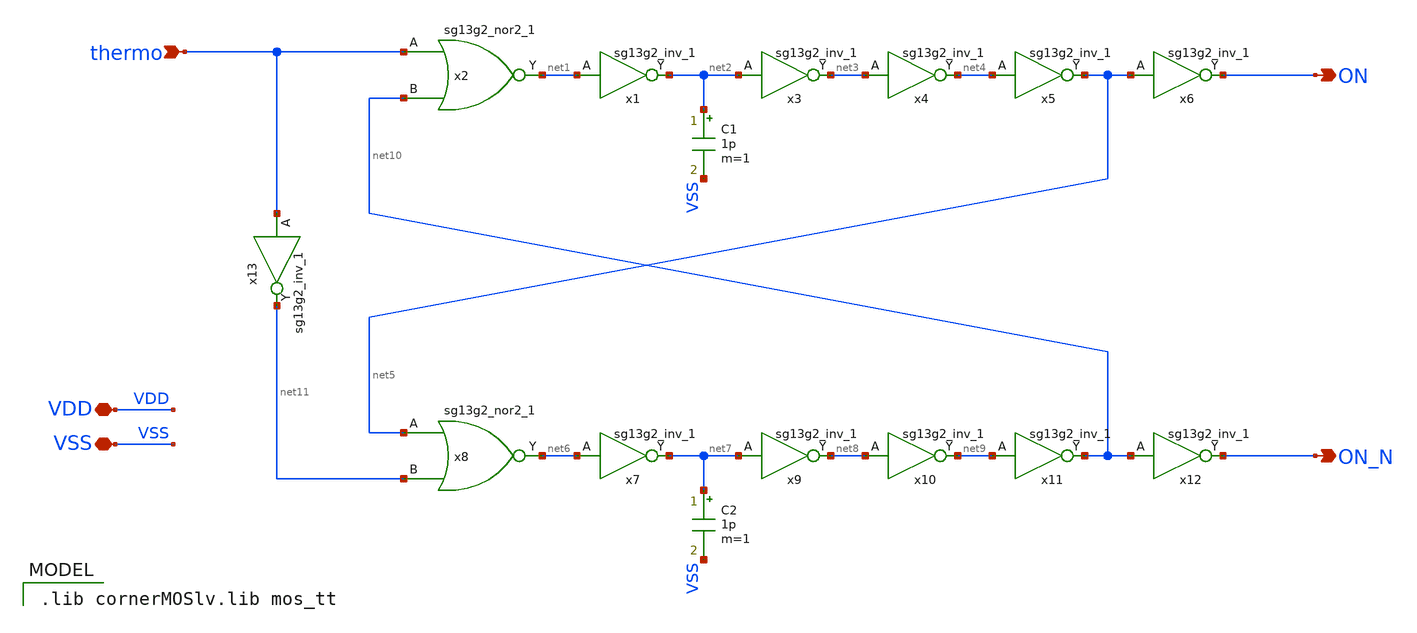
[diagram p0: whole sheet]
** sch_path: xschem/non_overlap.sch
* IHP-GmbH/IHP-Open-PDK/ihp-sg13g2/libs.tech/xschem/sg13g2_stdcells/sg13g2_nor2_1.sch:
* Copyright 2023 IHP PDK Authors
* Licensed under the Apache License, Version 2.0 (the "License");
**.subckt non_overlap VSS thermo ON ON_N VDD
*.iopin VSS
*.ipin thermo
*.opin ON
*.opin ON_N
*.iopin VDD
C1 net2 VSS 1p m=1
x1 net2 net1 VDD VSS sg13g2_inv_1
x2 net1 thermo net10 VDD VSS sg13g2_nor2_1
x3 net3 net2 VDD VSS sg13g2_inv_1
x4 net4 net3 VDD VSS sg13g2_inv_1
x5 net5 net4 VDD VSS sg13g2_inv_1
x6 ON net5 VDD VSS sg13g2_inv_1
C2 net7 VSS 1p m=1
x7 net7 net6 VDD VSS sg13g2_inv_1
x8 net6 net5 net11 VDD VSS sg13g2_nor2_1
x9 net8 net7 VDD VSS sg13g2_inv_1
x10 net9 net8 VDD VSS sg13g2_inv_1
x11 net10 net9 VDD VSS sg13g2_inv_1
x12 ON_N net10 VDD VSS sg13g2_inv_1
x13 net11 thermo VDD VSS sg13g2_inv_1
**** begin user architecture code
 .lib cornerMOSlv.lib mos_tt

**** end user architecture code
**.ends

* expanding   symbol:  sg13g2_stdcells/sg13g2_inv_1.sym # of pins=2
** sym_path: sg13g2_stdcells/sg13g2_inv_1.sym
** sch_path: sg13g2_stdcells/sg13g2_inv_1.sch
.subckt sg13g2_inv_1 Y A VDD VSS
*.opin Y
*.ipin A
*.iopin VDD
*.iopin VSS
XM1 Y A VSS VSS sg13_lv_nmos w=740.00n l=130.00n ng=1 m=1 mm_ok=1
XM2 Y A VDD VDD sg13_lv_pmos w=1.12u l=130.00n ng=1 m=1 mm_ok=1
.ends


* expanding   symbol:  sg13g2_stdcells/sg13g2_nor2_1.sym # of pins=3
** sym_path: sg13g2_stdcells/sg13g2_nor2_1.sym
** sch_path: sg13g2_stdcells/sg13g2_nor2_1.sch
.subckt sg13g2_nor2_1 Y A B VDD VSS
*.opin Y
*.ipin B
*.ipin A
*.iopin VDD
*.iopin VSS
XM1 Y A VSS VSS sg13_lv_nmos w=740.00n l=130.00n ng=1 m=1 mm_ok=1
XM2 Y B VSS VSS sg13_lv_nmos w=740.00n l=130.00n ng=1 m=1 mm_ok=1
XM3 net1 A VDD VDD sg13_lv_pmos w=1.12u l=130.00n ng=1 m=1 mm_ok=1
XM4 Y B net1 VDD sg13_lv_pmos w=1.12u l=130.00n ng=1 m=1 mm_ok=1
.ends

.end
